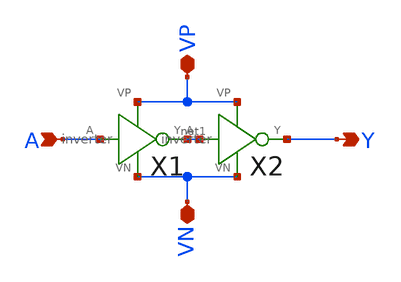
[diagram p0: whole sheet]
** sch_path: schematics/buffer.sch
**.subckt buffer A VP VN Y
*.ipin A
*.iopin VP
*.iopin VN
*.opin Y
X1 A net1 VP VN inverter
X2 net1 Y VP VN inverter
**.ends

* expanding   symbol:  /home/madvlsi/Documents/algorithmic-ada-converter/schematics/inverter.sym #
*+ of pins=4
** sym_path: schematics/inverter.sym
** sch_path: schematics/inverter.sch
.subckt inverter A Y VP VN
*.ipin A
*.iopin VP
*.iopin VN
*.opin Y
XM1 Y A VP VDD sky130_fd_pr__pfet_01v8 L=0.15 W=1 nf=1 ad='int((nf+1)/2) * W/nf * 0.29' as='int((nf+2)/2) * W/nf * 0.29'
+ pd='2*int((nf+1)/2) * (W/nf + 0.29)' ps='2*int((nf+2)/2) * (W/nf + 0.29)' nrd='0.29 / W' nrs='0.29 / W'
+ sa=0 sb=0 sd=0 mult=1 m=1
XM2 Y A VN GND sky130_fd_pr__nfet_01v8 L=0.15 W=1 nf=1 ad='int((nf+1)/2) * W/nf * 0.29' as='int((nf+2)/2) * W/nf * 0.29'
+ pd='2*int((nf+1)/2) * (W/nf + 0.29)' ps='2*int((nf+2)/2) * (W/nf + 0.29)' nrd='0.29 / W' nrs='0.29 / W'
+ sa=0 sb=0 sd=0 mult=1 m=1
.ends

.end
